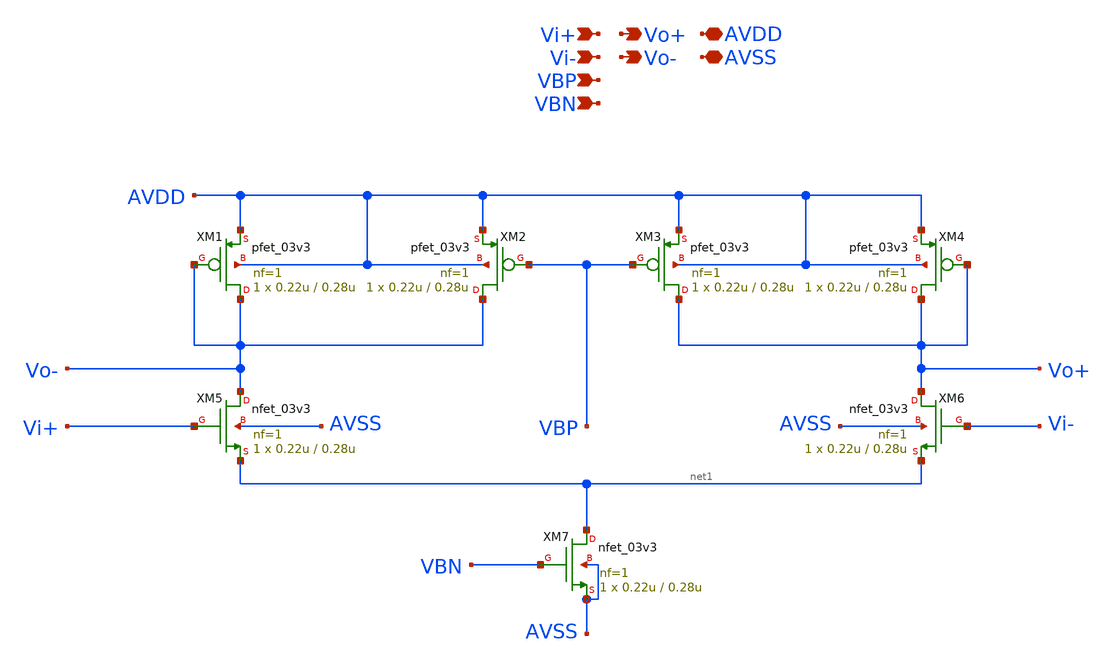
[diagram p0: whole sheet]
** sch_path: designs/libs/core_analog/delay_stage/delay_stage.sch
**.subckt delay_stage Vi+ Vi- Vo+ Vo- AVDD AVSS VBP VBN
*.ipin Vi+
*.ipin Vi-
*.opin Vo+
*.opin Vo-
*.iopin AVDD
*.iopin AVSS
*.ipin VBP
*.ipin VBN
XM1 Vo- Vo- AVDD AVDD pfet_03v3 L=0.28u W=0.22u nf=1 ad='int((nf+1)/2) * W/nf * 0.18u' as='int((nf+2)/2) * W/nf * 0.18u'
+ pd='2*int((nf+1)/2) * (W/nf + 0.18u)' ps='2*int((nf+2)/2) * (W/nf + 0.18u)' nrd='0.18u / W' nrs='0.18u / W'
+ sa=0 sb=0 sd=0 m=1
XM2 Vo- VBP AVDD AVDD pfet_03v3 L=0.28u W=0.22u nf=1 ad='int((nf+1)/2) * W/nf * 0.18u' as='int((nf+2)/2) * W/nf * 0.18u'
+ pd='2*int((nf+1)/2) * (W/nf + 0.18u)' ps='2*int((nf+2)/2) * (W/nf + 0.18u)' nrd='0.18u / W' nrs='0.18u / W'
+ sa=0 sb=0 sd=0 m=1
XM3 Vo+ VBP AVDD AVDD pfet_03v3 L=0.28u W=0.22u nf=1 ad='int((nf+1)/2) * W/nf * 0.18u' as='int((nf+2)/2) * W/nf * 0.18u'
+ pd='2*int((nf+1)/2) * (W/nf + 0.18u)' ps='2*int((nf+2)/2) * (W/nf + 0.18u)' nrd='0.18u / W' nrs='0.18u / W'
+ sa=0 sb=0 sd=0 m=1
XM4 Vo+ Vo+ AVDD AVDD pfet_03v3 L=0.28u W=0.22u nf=1 ad='int((nf+1)/2) * W/nf * 0.18u' as='int((nf+2)/2) * W/nf * 0.18u'
+ pd='2*int((nf+1)/2) * (W/nf + 0.18u)' ps='2*int((nf+2)/2) * (W/nf + 0.18u)' nrd='0.18u / W' nrs='0.18u / W'
+ sa=0 sb=0 sd=0 m=1
XM5 Vo- Vi+ net1 AVSS nfet_03v3 L=0.28u W=0.22u nf=1 ad='int((nf+1)/2) * W/nf * 0.18u' as='int((nf+2)/2) * W/nf * 0.18u'
+ pd='2*int((nf+1)/2) * (W/nf + 0.18u)' ps='2*int((nf+2)/2) * (W/nf + 0.18u)' nrd='0.18u / W' nrs='0.18u / W'
+ sa=0 sb=0 sd=0 m=1
XM6 Vo+ Vi- net1 AVSS nfet_03v3 L=0.28u W=0.22u nf=1 ad='int((nf+1)/2) * W/nf * 0.18u' as='int((nf+2)/2) * W/nf * 0.18u'
+ pd='2*int((nf+1)/2) * (W/nf + 0.18u)' ps='2*int((nf+2)/2) * (W/nf + 0.18u)' nrd='0.18u / W' nrs='0.18u / W'
+ sa=0 sb=0 sd=0 m=1
XM7 net1 VBN AVSS AVSS nfet_03v3 L=0.28u W=0.22u nf=1 ad='int((nf+1)/2) * W/nf * 0.18u' as='int((nf+2)/2) * W/nf * 0.18u'
+ pd='2*int((nf+1)/2) * (W/nf + 0.18u)' ps='2*int((nf+2)/2) * (W/nf + 0.18u)' nrd='0.18u / W' nrs='0.18u / W'
+ sa=0 sb=0 sd=0 m=1
**.ends
.end
